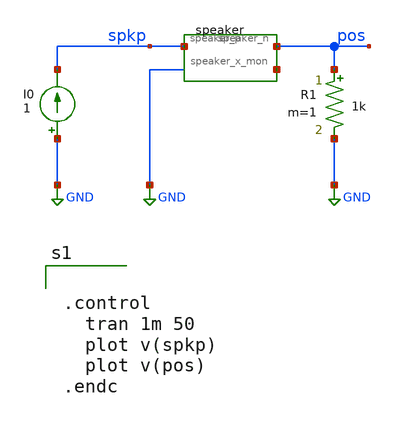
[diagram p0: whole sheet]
** sch_path: examples/analog_speaker/dc.sch
**.subckt dc
Xspeaker1 spkp pos net1 speaker
R1 pos GND 1k m=1
I0 GND spkp 1
**** begin user architecture code


.control
  tran 1m 50
  plot v(spkp)
  plot v(pos)
.endc


**** end user architecture code
**.ends

* expanding   symbol:  speaker.sym # of pins=3
** sym_path: examples/analog_speaker/speaker.sym
.include /workspace/speaker.spice
.GLOBAL GND
.end
